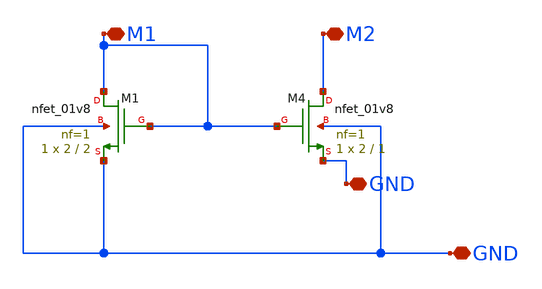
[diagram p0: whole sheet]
** sch_path: nmos.sch
**.subckt nmos M1 M2 GND GND
*.iopin M1
*.iopin M2
*.iopin GND
*.iopin GND
XM1 M1 M1 GND GND sky130_fd_pr__nfet_01v8 L=2 W=2 nf=1 ad='int((nf+1)/2) * W/nf * 0.29' as='int((nf+2)/2) * W/nf * 0.29'
+ pd='2*int((nf+1)/2) * (W/nf + 0.29)' ps='2*int((nf+2)/2) * (W/nf + 0.29)' nrd='0.29 / W' nrs='0.29 / W'
+ sa=0 sb=0 sd=0 mult=1 m=1
XM4 M2 M1 GND GND sky130_fd_pr__nfet_01v8 L=1 W=2 nf=1 ad='int((nf+1)/2) * W/nf * 0.29' as='int((nf+2)/2) * W/nf * 0.29'
+ pd='2*int((nf+1)/2) * (W/nf + 0.29)' ps='2*int((nf+2)/2) * (W/nf + 0.29)' nrd='0.29 / W' nrs='0.29 / W'
+ sa=0 sb=0 sd=0 mult=1 m=1
**.ends
.end
